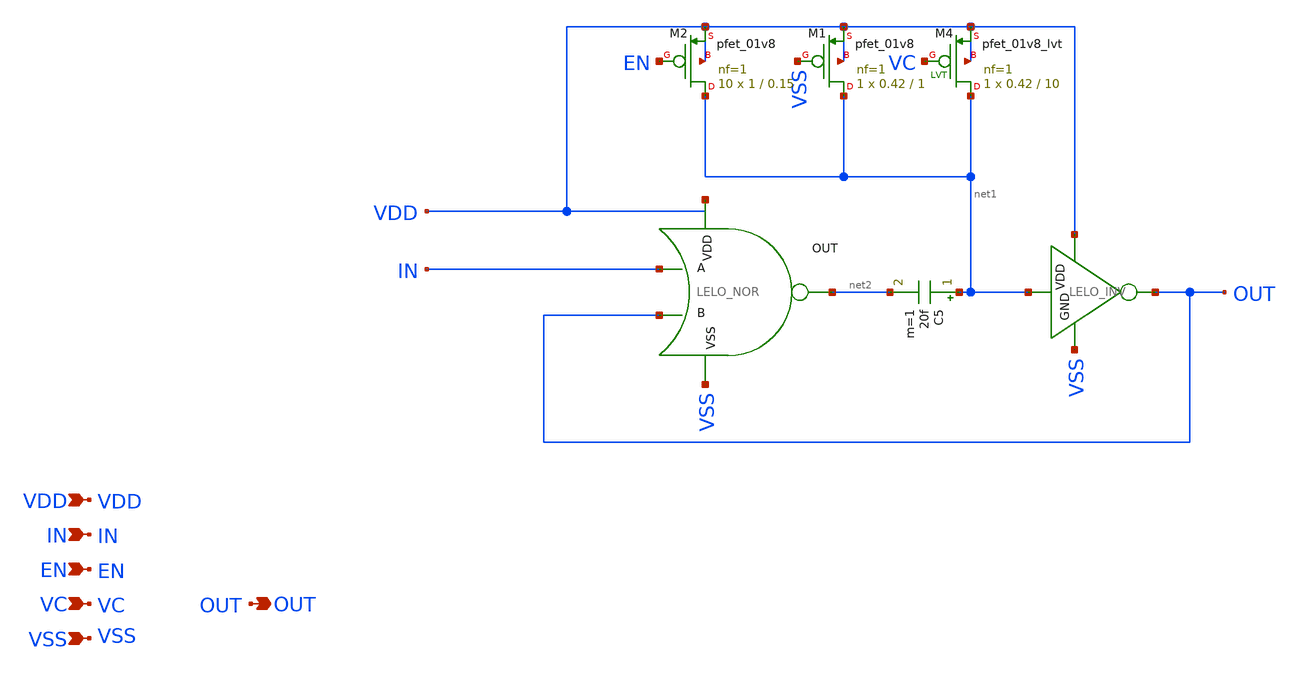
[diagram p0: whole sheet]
** sch_path: design/LELO_SVOD_SKY130A/LELO_ONESHOT_VC.sch
**.subckt LELO_ONESHOT_VC VDD IN VC VSS OUT EN
*.ipin VDD
*.ipin IN
*.ipin VC
*.ipin VSS
*.opin OUT
*.ipin EN
x2 net3 net2 IN OUT VSS LELO_NOR
C5 net1 net2 20f m=1
x3 VDD net1 OUT VSS LELO_INV
XM4 net1 VC VDD VDD sky130_fd_pr__pfet_01v8_lvt L=10 W=0.42 nf=1 ad='int((1 + 1)/2) * 0.42 / 1 * 0.29'
+ as='int((1 + 2)/2) * 0.42 / 1 * 0.29' pd='2*int((1 + 1)/2) * (0.42 / 1 + 0.29)' ps='2*int((1 + 2)/2) * (0.42 / 1 + 0.29)'
+ nrd='0.29 / 0.42 ' nrs='0.29 / 0.42 ' sa=0 sb=0 sd=0 mult=1 m=1
XM1 net1 VSS VDD VDD sky130_fd_pr__pfet_01v8 L=1 W=0.42 nf=1 ad='int((1 + 1)/2) * 0.42 / 1 * 0.29' as='int((1 + 2)/2) * 0.42 / 1 * 0.29'
+ pd='2*int((1 + 1)/2) * (0.42 / 1 + 0.29)' ps='2*int((1 + 2)/2) * (0.42 / 1 + 0.29)' nrd='0.29 / 0.42 '
+ nrs='0.29 / 0.42 ' sa=0 sb=0 sd=0 mult=1 m=1
XM2 net1 EN VDD VDD sky130_fd_pr__pfet_01v8 L=0.15 W=1 nf=1 ad='int((1 + 1)/2) * 1 / 1 * 0.29' as='int((1 + 2)/2) * 1 / 1 * 0.29'
+ pd='2*int((1 + 1)/2) * (1 / 1 + 0.29)' ps='2*int((1 + 2)/2) * (1 / 1 + 0.29)' nrd='0.29 / 1 ' nrs='0.29 / 1 '
+ sa=0 sb=0 sd=0 mult=10 m=10
**.ends

* expanding   symbol:  LELO_SVOD_SKY130A/LELO_NOR.sym # of pins=5
** sym_path: design/LELO_SVOD_SKY130A/LELO_NOR.sym
** sch_path: design/LELO_SVOD_SKY130A/LELO_NOR.sch
.subckt LELO_NOR VDD OUT A B VSS
*.ipin VDD
*.ipin VSS
*.opin OUT
*.ipin A
*.ipin B
XM2 OUT B VSS VSS sky130_fd_pr__nfet_01v8 L=0.15 W=2 nf=1 ad='int((1 + 1)/2) * 2 / 1 * 0.29' as='int((1 + 2)/2) * 2 / 1 * 0.29'
+ pd='2*int((1 + 1)/2) * (2 / 1 + 0.29)' ps='2*int((1 + 2)/2) * (2 / 1 + 0.29)' nrd='0.29 / 2 ' nrs='0.29 / 2 '
+ sa=0 sb=0 sd=0 mult=1 m=1
XM1 OUT A VSS VSS sky130_fd_pr__nfet_01v8 L=0.15 W=2 nf=1 ad='int((1 + 1)/2) * 2 / 1 * 0.29' as='int((1 + 2)/2) * 2 / 1 * 0.29'
+ pd='2*int((1 + 1)/2) * (2 / 1 + 0.29)' ps='2*int((1 + 2)/2) * (2 / 1 + 0.29)' nrd='0.29 / 2 ' nrs='0.29 / 2 '
+ sa=0 sb=0 sd=0 mult=1 m=1
XM3 OUT B net1 VDD sky130_fd_pr__pfet_01v8 L=0.15 W=4 nf=1 ad='int((1 + 1)/2) * 4 / 1 * 0.29' as='int((1 + 2)/2) * 4 / 1 * 0.29'
+ pd='2*int((1 + 1)/2) * (4 / 1 + 0.29)' ps='2*int((1 + 2)/2) * (4 / 1 + 0.29)' nrd='0.29 / 4 ' nrs='0.29 / 4 '
+ sa=0 sb=0 sd=0 mult=1 m=1
XM4 net1 A VDD VDD sky130_fd_pr__pfet_01v8 L=0.15 W=4 nf=1 ad='int((1 + 1)/2) * 4 / 1 * 0.29' as='int((1 + 2)/2) * 4 / 1 * 0.29'
+ pd='2*int((1 + 1)/2) * (4 / 1 + 0.29)' ps='2*int((1 + 2)/2) * (4 / 1 + 0.29)' nrd='0.29 / 4 ' nrs='0.29 / 4 '
+ sa=0 sb=0 sd=0 mult=1 m=1
.ends


* expanding   symbol:  LELO_SVOD_SKY130A/LELO_INV.sym # of pins=4
** sym_path: design/LELO_SVOD_SKY130A/LELO_INV.sym
** sch_path: design/LELO_SVOD_SKY130A/LELO_INV.sch
.subckt LELO_INV VDD VIN VOUT GND
*.ipin VIN
*.ipin VDD
*.ipin GND
*.opin VOUT
XM1 VOUT VIN GND GND sky130_fd_pr__nfet_01v8_lvt L=0.15 W=1 nf=1 ad='int((1 + 1)/2) * 1 / 1 * 0.29' as='int((1 + 2)/2) * 1 / 1 * 0.29'
+ pd='2*int((1 + 1)/2) * (1 / 1 + 0.29)' ps='2*int((1 + 2)/2) * (1 / 1 + 0.29)' nrd='0.29 / 1 ' nrs='0.29 / 1 '
+ sa=0 sb=0 sd=0 mult=1 m=1
XM2 VOUT VIN VDD VDD sky130_fd_pr__pfet_01v8_lvt L=0.35 W=1 nf=1 ad='int((1 + 1)/2) * 1 / 1 * 0.29' as='int((1 + 2)/2) * 1 / 1 * 0.29'
+ pd='2*int((1 + 1)/2) * (1 / 1 + 0.29)' ps='2*int((1 + 2)/2) * (1 / 1 + 0.29)' nrd='0.29 / 1 ' nrs='0.29 / 1 '
+ sa=0 sb=0 sd=0 mult=2 m=2
.ends

.end
